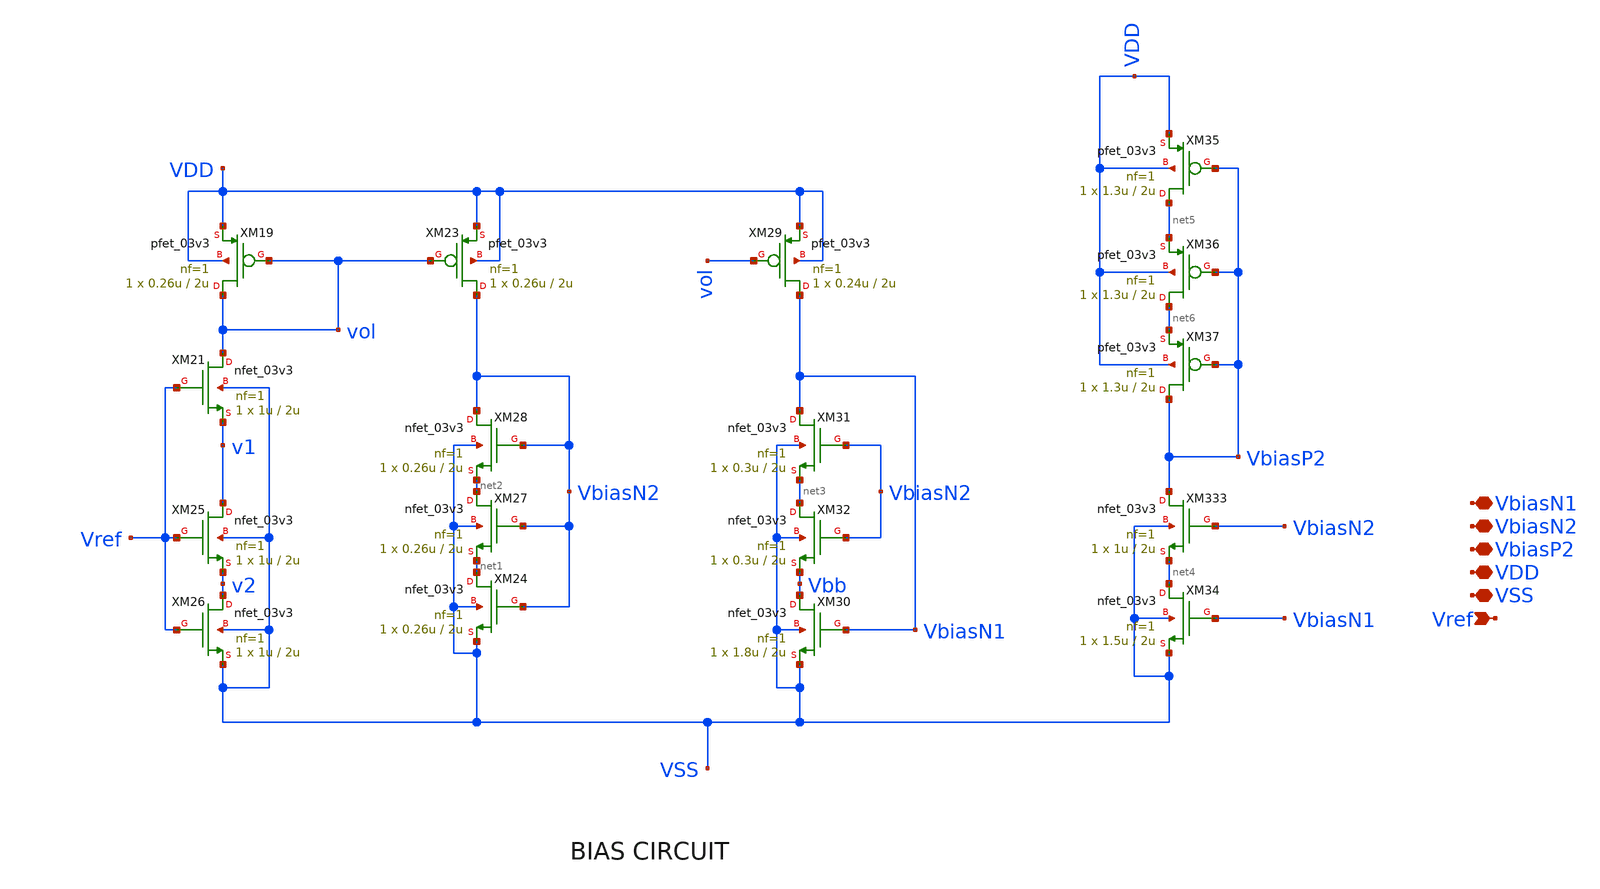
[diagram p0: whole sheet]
** sch_path: designs/used_and_to_delete/error_amplifier_bias_bradly/xschem/error_amplifier_bias_bradly.sch
**.subckt error_amplifier_bias_bradly Vref VbiasN1 VbiasN2 VDD VbiasP2 VSS
*.ipin Vref
*.iopin VbiasN1
*.iopin VbiasN2
*.iopin VDD
*.iopin VbiasP2
*.iopin VSS
XM19 vol vol VDD VDD pfet_03v3 L=2u W=0.26u nf=1 ad='int((nf+1)/2) * W/nf * 0.18u' as='int((nf+2)/2) * W/nf * 0.18u'
+ pd='2*int((nf+1)/2) * (W/nf + 0.18u)' ps='2*int((nf+2)/2) * (W/nf + 0.18u)' nrd='0.18u / W' nrs='0.18u / W'
+ sa=0 sb=0 sd=0 m=1
XM21 vol Vref v1 VSS nfet_03v3 L=2u W=1u nf=1 ad='int((nf+1)/2) * W/nf * 0.18u' as='int((nf+2)/2) * W/nf * 0.18u'
+ pd='2*int((nf+1)/2) * (W/nf + 0.18u)' ps='2*int((nf+2)/2) * (W/nf + 0.18u)' nrd='0.18u / W' nrs='0.18u / W'
+ sa=0 sb=0 sd=0 m=1
XM23 VbiasN2 vol VDD VDD pfet_03v3 L=2u W=0.26u nf=1 ad='int((nf+1)/2) * W/nf * 0.18u' as='int((nf+2)/2) * W/nf * 0.18u'
+ pd='2*int((nf+1)/2) * (W/nf + 0.18u)' ps='2*int((nf+2)/2) * (W/nf + 0.18u)' nrd='0.18u / W' nrs='0.18u / W'
+ sa=0 sb=0 sd=0 m=1
XM24 net1 VbiasN2 VSS VSS nfet_03v3 L=2u W=0.26u nf=1 ad='int((nf+1)/2) * W/nf * 0.18u' as='int((nf+2)/2) * W/nf * 0.18u'
+ pd='2*int((nf+1)/2) * (W/nf + 0.18u)' ps='2*int((nf+2)/2) * (W/nf + 0.18u)' nrd='0.18u / W' nrs='0.18u / W'
+ sa=0 sb=0 sd=0 m=1
XM25 v1 Vref v2 VSS nfet_03v3 L=2u W=1u nf=1 ad='int((nf+1)/2) * W/nf * 0.18u' as='int((nf+2)/2) * W/nf * 0.18u'
+ pd='2*int((nf+1)/2) * (W/nf + 0.18u)' ps='2*int((nf+2)/2) * (W/nf + 0.18u)' nrd='0.18u / W' nrs='0.18u / W'
+ sa=0 sb=0 sd=0 m=1
XM26 v2 Vref VSS VSS nfet_03v3 L=2u W=1u nf=1 ad='int((nf+1)/2) * W/nf * 0.18u' as='int((nf+2)/2) * W/nf * 0.18u'
+ pd='2*int((nf+1)/2) * (W/nf + 0.18u)' ps='2*int((nf+2)/2) * (W/nf + 0.18u)' nrd='0.18u / W' nrs='0.18u / W'
+ sa=0 sb=0 sd=0 m=1
XM27 net2 VbiasN2 net1 VSS nfet_03v3 L=2u W=0.26u nf=1 ad='int((nf+1)/2) * W/nf * 0.18u' as='int((nf+2)/2) * W/nf * 0.18u'
+ pd='2*int((nf+1)/2) * (W/nf + 0.18u)' ps='2*int((nf+2)/2) * (W/nf + 0.18u)' nrd='0.18u / W' nrs='0.18u / W'
+ sa=0 sb=0 sd=0 m=1
XM28 VbiasN2 VbiasN2 net2 VSS nfet_03v3 L=2u W=0.26u nf=1 ad='int((nf+1)/2) * W/nf * 0.18u' as='int((nf+2)/2) * W/nf * 0.18u'
+ pd='2*int((nf+1)/2) * (W/nf + 0.18u)' ps='2*int((nf+2)/2) * (W/nf + 0.18u)' nrd='0.18u / W' nrs='0.18u / W'
+ sa=0 sb=0 sd=0 m=1
XM29 VbiasN1 vol VDD VDD pfet_03v3 L=2u W=0.24u nf=1 ad='int((nf+1)/2) * W/nf * 0.18u' as='int((nf+2)/2) * W/nf * 0.18u'
+ pd='2*int((nf+1)/2) * (W/nf + 0.18u)' ps='2*int((nf+2)/2) * (W/nf + 0.18u)' nrd='0.18u / W' nrs='0.18u / W'
+ sa=0 sb=0 sd=0 m=1
XM30 Vbb VbiasN1 VSS VSS nfet_03v3 L=2u W=1.8u nf=1 ad='int((nf+1)/2) * W/nf * 0.18u' as='int((nf+2)/2) * W/nf * 0.18u'
+ pd='2*int((nf+1)/2) * (W/nf + 0.18u)' ps='2*int((nf+2)/2) * (W/nf + 0.18u)' nrd='0.18u / W' nrs='0.18u / W'
+ sa=0 sb=0 sd=0 m=1
XM31 VbiasN1 VbiasN2 net3 VSS nfet_03v3 L=2u W=0.3u nf=1 ad='int((nf+1)/2) * W/nf * 0.18u' as='int((nf+2)/2) * W/nf * 0.18u'
+ pd='2*int((nf+1)/2) * (W/nf + 0.18u)' ps='2*int((nf+2)/2) * (W/nf + 0.18u)' nrd='0.18u / W' nrs='0.18u / W'
+ sa=0 sb=0 sd=0 m=1
XM32 net3 VbiasN2 Vbb VSS nfet_03v3 L=2u W=0.3u nf=1 ad='int((nf+1)/2) * W/nf * 0.18u' as='int((nf+2)/2) * W/nf * 0.18u'
+ pd='2*int((nf+1)/2) * (W/nf + 0.18u)' ps='2*int((nf+2)/2) * (W/nf + 0.18u)' nrd='0.18u / W' nrs='0.18u / W'
+ sa=0 sb=0 sd=0 m=1
XM333 VbiasP2 VbiasN2 net4 VSS nfet_03v3 L=2u W=1u nf=1 ad='int((nf+1)/2) * W/nf * 0.18u' as='int((nf+2)/2) * W/nf * 0.18u'
+ pd='2*int((nf+1)/2) * (W/nf + 0.18u)' ps='2*int((nf+2)/2) * (W/nf + 0.18u)' nrd='0.18u / W' nrs='0.18u / W'
+ sa=0 sb=0 sd=0 m=1
XM34 net4 VbiasN1 VSS VSS nfet_03v3 L=2u W=1.5u nf=1 ad='int((nf+1)/2) * W/nf * 0.18u' as='int((nf+2)/2) * W/nf * 0.18u'
+ pd='2*int((nf+1)/2) * (W/nf + 0.18u)' ps='2*int((nf+2)/2) * (W/nf + 0.18u)' nrd='0.18u / W' nrs='0.18u / W'
+ sa=0 sb=0 sd=0 m=1
XM35 net5 VbiasP2 VDD VDD pfet_03v3 L=2u W=1.3u nf=1 ad='int((nf+1)/2) * W/nf * 0.18u' as='int((nf+2)/2) * W/nf * 0.18u'
+ pd='2*int((nf+1)/2) * (W/nf + 0.18u)' ps='2*int((nf+2)/2) * (W/nf + 0.18u)' nrd='0.18u / W' nrs='0.18u / W'
+ sa=0 sb=0 sd=0 m=1
XM36 net6 VbiasP2 net5 VDD pfet_03v3 L=2u W=1.3u nf=1 ad='int((nf+1)/2) * W/nf * 0.18u' as='int((nf+2)/2) * W/nf * 0.18u'
+ pd='2*int((nf+1)/2) * (W/nf + 0.18u)' ps='2*int((nf+2)/2) * (W/nf + 0.18u)' nrd='0.18u / W' nrs='0.18u / W'
+ sa=0 sb=0 sd=0 m=1
XM37 VbiasP2 VbiasP2 net6 VDD pfet_03v3 L=2u W=1.3u nf=1 ad='int((nf+1)/2) * W/nf * 0.18u' as='int((nf+2)/2) * W/nf * 0.18u'
+ pd='2*int((nf+1)/2) * (W/nf + 0.18u)' ps='2*int((nf+2)/2) * (W/nf + 0.18u)' nrd='0.18u / W' nrs='0.18u / W'
+ sa=0 sb=0 sd=0 m=1
**.ends
.end
